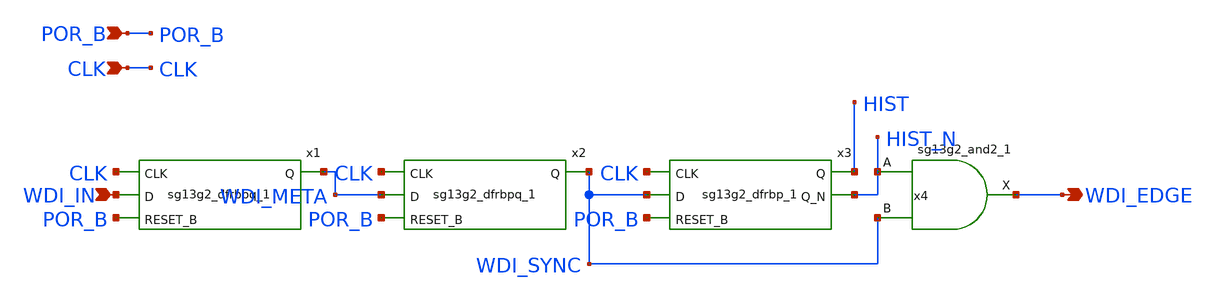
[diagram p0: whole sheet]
** sch_path: design/blocks/wd_input/schematic/WDI_INPUT.sch
**.subckt WDI_INPUT WDI_EDGE WDI_IN POR_B CLK
*.opin WDI_EDGE
*.ipin WDI_IN
*.ipin POR_B
*.ipin CLK
x1 WDI_META CLK WDI_IN POR_B VDD VSS sg13g2_dfrbpq_1
x2 WDI_SYNC CLK WDI_META POR_B VDD VSS sg13g2_dfrbpq_1
x4 WDI_EDGE HIST_N WDI_SYNC VDD VSS sg13g2_and2_1
x3 HIST HIST_N CLK WDI_SYNC POR_B VDD VSS sg13g2_dfrbp_1
**.ends

* expanding   symbol:  sg13g2_dfrbpq_1.sym # of pins=4
** sym_path: sg13g2_dfrbpq_1.sym
** sch_path: sg13g2_dfrbpq_1.sch
.subckt sg13g2_dfrbpq_1 Q CLK D RESET_B VDD VSS
*.opin Q
*.ipin CLK
*.ipin D
*.ipin RESET_B
*.iopin VDD
*.iopin VSS
XM1 Db D net10 VSS sg13_lv_nmos w=420.00n l=130.00n ng=1 m=1 mm_ok=1
XM2 net10 RESET_B VSS VSS sg13_lv_nmos w=420.00n l=130.00n ng=1 m=1 mm_ok=1
XM3 net1 clkneg net9 VSS sg13_lv_nmos w=420.00n l=130.00n ng=1 m=1 mm_ok=1
XM4 net9 net1 VSS VSS sg13_lv_nmos w=420.00n l=130.00n ng=1 m=1 mm_ok=1
XM5 net1 net1 net5 VSS sg13_lv_nmos w=420.00n l=130.00n ng=1 m=1 mm_ok=1
XM6 net5 RESET_B VSS VSS sg13_lv_nmos w=420.00n l=130.00n ng=1 m=1 mm_ok=1
XM7 net2 net1 VSS VSS sg13_lv_nmos w=740.00n l=130.00n ng=1 m=1 mm_ok=1
XM8 Q net2 VSS VSS sg13_lv_nmos w=740.00n l=130.00n ng=1 m=1 mm_ok=1
XM9 clkneg CLK VSS VSS sg13_lv_nmos w=740.00n l=130.00n ng=1 m=1 mm_ok=1
XM10 clkpos clkneg VSS VSS sg13_lv_nmos w=740.00n l=130.00n ng=1 m=1 mm_ok=1
XM11 Db clkneg net3 VSS sg13_lv_nmos w=420.00n l=130.00n ng=1 m=1 mm_ok=1
XM12 net3 clkpos net8 VSS sg13_lv_nmos w=420.00n l=130.00n ng=1 m=1 mm_ok=1
XM13 net8 net3 net4 VSS sg13_lv_nmos w=420.00n l=130.00n ng=1 m=1 mm_ok=1
XM14 net4 RESET_B VSS VSS sg13_lv_nmos w=420.00n l=130.00n ng=1 m=1 mm_ok=1
XM15 net3 net3 VSS VSS sg13_lv_nmos w=740.00n l=130.00n ng=1 m=1 mm_ok=1
XM16 net3 clkpos net1 VSS sg13_lv_nmos w=740.00n l=130.00n ng=1 m=1 mm_ok=1
XM17 Db RESET_B VDD VDD sg13_lv_pmos w=420.00n l=130.00n ng=1 m=1 mm_ok=1
XM18 Db D VDD VDD sg13_lv_pmos w=420.00n l=130.00n ng=1 m=1 mm_ok=1
XM19 net7 net1 VDD VDD sg13_lv_pmos w=420.00n l=130.00n ng=1 m=1 mm_ok=1
XM20 net1 clkpos net7 VDD sg13_lv_pmos w=420.00n l=130.00n ng=1 m=1 mm_ok=1
XM21 net1 net1 VDD VDD sg13_lv_pmos w=420.00n l=130.00n ng=1 m=1 mm_ok=1
XM22 net1 RESET_B VDD VDD sg13_lv_pmos w=420.00n l=130.00n ng=1 m=1 mm_ok=1
XM23 net2 net1 VDD VDD sg13_lv_pmos w=1.12u l=130.00n ng=1 m=1 mm_ok=1
XM24 Q net2 VDD VDD sg13_lv_pmos w=1.12u l=130.00n ng=1 m=1 mm_ok=1
XM25 clkneg CLK VDD VDD sg13_lv_pmos w=1.12u l=130.00n ng=1 m=1 mm_ok=1
XM26 clkpos clkneg VDD VDD sg13_lv_pmos w=1.12u l=130.00n ng=1 m=1 mm_ok=1
XM27 Db clkpos net3 VDD sg13_lv_pmos w=420.00n l=130.00n ng=1 m=1 mm_ok=1
XM28 net6 net3 VDD VDD sg13_lv_pmos w=420.00n l=130.00n ng=1 m=1 mm_ok=1
XM29 net3 clkneg net6 VDD sg13_lv_pmos w=420.00n l=130.00n ng=1 m=1 mm_ok=1
XM30 net3 RESET_B VDD VDD sg13_lv_pmos w=420.00n l=130.00n ng=1 m=1 mm_ok=1
XM31 net3 net3 VDD VDD sg13_lv_pmos w=1.000u l=130.00n ng=1 m=1 mm_ok=1
XM32 net3 clkneg net1 VDD sg13_lv_pmos w=1.000u l=130.00n ng=1 m=1 mm_ok=1
.ends


* expanding   symbol:  sg13g2_and2_1.sym # of pins=3
** sym_path: sg13g2_and2_1.sym
** sch_path: sg13g2_and2_1.sch
.subckt sg13g2_and2_1 X A B VDD VSS
*.ipin A
*.ipin B
*.opin X
*.iopin VDD
*.iopin VSS
XM1 net1 A net2 VSS sg13_lv_nmos w=640.00n l=130.00n ng=1 m=1 mm_ok=1
XM2 net2 B VSS VSS sg13_lv_nmos w=640.00n l=130.00n ng=1 m=1 mm_ok=1
XM3 X net1 VSS VSS sg13_lv_nmos w=740.00n l=130.00n ng=1 m=1 mm_ok=1
XM4 net1 B VDD VDD sg13_lv_pmos w=840.00n l=130.00n ng=1 m=1 mm_ok=1
XM5 net1 A VDD VDD sg13_lv_pmos w=840.00n l=130.00n ng=1 m=1 mm_ok=1
XM6 X net1 VDD VDD sg13_lv_pmos w=1.12u l=130.00n ng=1 m=1 mm_ok=1
.ends


* expanding   symbol:  sg13g2_dfrbp_1.sym # of pins=5
** sym_path: sg13g2_dfrbp_1.sym
** sch_path: sg13g2_dfrbp_1.sch
.subckt sg13g2_dfrbp_1 Q Q_N CLK D RESET_B VDD VSS
*.ipin D
*.ipin RESET_B
*.ipin CLK
*.opin Q
*.opin Q_N
*.iopin VDD
*.iopin VSS
XM1 Db D net10 VSS sg13_lv_nmos w=420.00n l=130.00n ng=1 m=1 mm_ok=1
XM2 net10 RESET_B VSS VSS sg13_lv_nmos w=420.00n l=130.00n ng=1 m=1 mm_ok=1
XM3 net1 clkneg net9 VSS sg13_lv_nmos w=420.00n l=130.00n ng=1 m=1 mm_ok=1
XM4 net9 net1 VSS VSS sg13_lv_nmos w=420.00n l=130.00n ng=1 m=1 mm_ok=1
XM5 net1 net1 net5 VSS sg13_lv_nmos w=420.00n l=130.00n ng=1 m=1 mm_ok=1
XM6 net5 RESET_B VSS VSS sg13_lv_nmos w=420.00n l=130.00n ng=1 m=1 mm_ok=1
XM7 Q_N net1 VSS VSS sg13_lv_nmos w=740.00n l=130.00n ng=1 m=1 mm_ok=1
XM8 net2 net1 VSS VSS sg13_lv_nmos w=740.00n l=130.00n ng=1 m=1 mm_ok=1
XM9 Q net2 VSS VSS sg13_lv_nmos w=740.00n l=130.00n ng=1 m=1 mm_ok=1
XM10 clkneg CLK VSS VSS sg13_lv_nmos w=740.00n l=130.00n ng=1 m=1 mm_ok=1
XM11 clkpos clkneg VSS VSS sg13_lv_nmos w=740.00n l=130.00n ng=1 m=1 mm_ok=1
XM12 Db clkneg net3 VSS sg13_lv_nmos w=420.00n l=130.00n ng=1 m=1 mm_ok=1
XM13 net3 clkpos net8 VSS sg13_lv_nmos w=420.00n l=130.00n ng=1 m=1 mm_ok=1
XM14 net8 net3 net4 VSS sg13_lv_nmos w=420.00n l=130.00n ng=1 m=1 mm_ok=1
XM15 net4 RESET_B VSS VSS sg13_lv_nmos w=420.00n l=130.00n ng=1 m=1 mm_ok=1
XM16 net3 net3 VSS VSS sg13_lv_nmos w=740.00n l=130.00n ng=1 m=1 mm_ok=1
XM17 net3 clkpos net1 VSS sg13_lv_nmos w=740.00n l=130.00n ng=1 m=1 mm_ok=1
XM18 Db RESET_B VDD VDD sg13_lv_pmos w=420.00n l=130.00n ng=1 m=1 mm_ok=1
XM19 Db D VDD VDD sg13_lv_pmos w=420.00n l=130.00n ng=1 m=1 mm_ok=1
XM20 net7 net1 VDD VDD sg13_lv_pmos w=420.00n l=130.00n ng=1 m=1 mm_ok=1
XM21 net1 clkpos net7 VDD sg13_lv_pmos w=420.00n l=130.00n ng=1 m=1 mm_ok=1
XM22 net1 net1 VDD VDD sg13_lv_pmos w=420.00n l=130.00n ng=1 m=1 mm_ok=1
XM23 net1 RESET_B VDD VDD sg13_lv_pmos w=420.00n l=130.00n ng=1 m=1 mm_ok=1
XM24 Q_N net1 VDD VDD sg13_lv_pmos w=1.12u l=130.00n ng=1 m=1 mm_ok=1
XM25 net2 net1 VDD VDD sg13_lv_pmos w=1.12u l=130.00n ng=1 m=1 mm_ok=1
XM26 Q net2 VDD VDD sg13_lv_pmos w=1.12u l=130.00n ng=1 m=1 mm_ok=1
XM27 clkneg CLK VDD VDD sg13_lv_pmos w=1.12u l=130.00n ng=1 m=1 mm_ok=1
XM28 clkpos clkneg VDD VDD sg13_lv_pmos w=1.12u l=130.00n ng=1 m=1 mm_ok=1
XM29 Db clkpos net3 VDD sg13_lv_pmos w=420.00n l=130.00n ng=1 m=1 mm_ok=1
XM30 net6 net3 VDD VDD sg13_lv_pmos w=420.00n l=130.00n ng=1 m=1 mm_ok=1
XM31 net3 clkneg net6 VDD sg13_lv_pmos w=420.00n l=130.00n ng=1 m=1 mm_ok=1
XM32 net3 RESET_B VDD VDD sg13_lv_pmos w=420.00n l=130.00n ng=1 m=1 mm_ok=1
XM33 net3 net3 VDD VDD sg13_lv_pmos w=1.000u l=130.00n ng=1 m=1 mm_ok=1
XM34 net3 clkneg net1 VDD sg13_lv_pmos w=1.000u l=130.00n ng=1 m=1 mm_ok=1
.ends

.end
